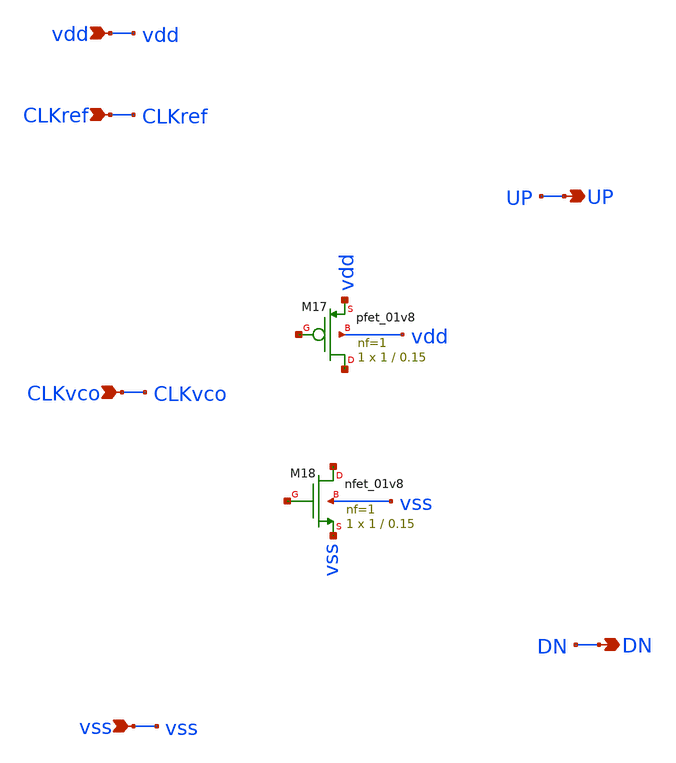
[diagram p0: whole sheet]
** sch_path: src/Dff.sch
**.subckt Dff UP CLKref CLKvco DN vdd vss
*.opin UP
*.ipin CLKref
*.ipin CLKvco
*.opin DN
*.ipin vdd
*.ipin vss
XM17 net1 net2 vdd vdd sky130_fd_pr__pfet_01v8 L=0.15 W=1 nf=1 ad='int((1 + 1)/2) * 1 / 1 * 0.29' as='int((1 + 2)/2) * 1 / 1 * 0.29'
+ pd='2*int((1 + 1)/2) * (1 / 1 + 0.29)' ps='2*int((1 + 2)/2) * (1 / 1 + 0.29)' nrd='0.29 / 1 ' nrs='0.29 / 1 '
+ sa=0 sb=0 sd=0 mult=1 m=1
XM18 net3 net4 vss vss sky130_fd_pr__nfet_01v8 L=0.15 W=1 nf=1 ad='int((1 + 1)/2) * 1 / 1 * 0.29' as='int((1 + 2)/2) * 1 / 1 * 0.29'
+ pd='2*int((1 + 1)/2) * (1 / 1 + 0.29)' ps='2*int((1 + 2)/2) * (1 / 1 + 0.29)' nrd='0.29 / 1 ' nrs='0.29 / 1 '
+ sa=0 sb=0 sd=0 mult=1 m=1
**** begin user architecture code


.option temp=27

* power supplies
VDD vdd 0 1.8
VSS vss 0 0


* reference clock (20 ns period = 50 MHz)
Vref CLKref 0 pulse(0 1.8 0 1n 1n 10n 20n)

* VCO clock (slightly different frequency, 19 ns period ~52.6 MHz)
Vvco CLKvco 0 pulse(0 1.8 0 1n 1n 9.5n 19n)

* analysis
.tran 0.1n 500n
.control
run
plot v(CLKref) v(CLKvco) v(UP)+2 v(DN)+4

.endc



** opencircuitdesign pdks install
.lib $::SKYWATER_MODELS/sky130.lib.spice tt


**** end user architecture code
**.ends
.end
